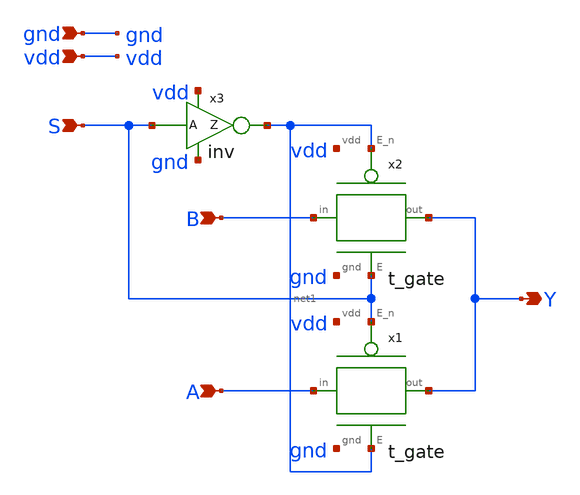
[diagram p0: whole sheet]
** sch_path: xschem/mux21.sch
**.subckt mux21 S A B Y vdd gnd
*.ipin S
*.ipin A
*.ipin B
*.opin Y
*.ipin vdd
*.ipin gnd
x1 S A Y net1 vdd gnd t_gate
x2 net1 B Y S vdd gnd t_gate
x3 net1 S vdd gnd inv
**.ends

* expanding   symbol:  t_gate.sym # of pins=6
** sym_path: xschem/t_gate.sym
** sch_path: xschem/t_gate.sch
.subckt t_gate E_n in out E vdd gnd
*.ipin in
*.opin out
*.ipin E
*.ipin E_n
*.ipin vdd
*.ipin gnd
XM1 in E out gnd sky130_fd_pr__nfet_01v8 L=0.15 W=0.42 nf=1 ad='int((nf+1)/2) * W/nf * 0.29' as='int((nf+2)/2) * W/nf * 0.29'
+ pd='2*int((nf+1)/2) * (W/nf + 0.29)' ps='2*int((nf+2)/2) * (W/nf + 0.29)' nrd='0.29 / W' nrs='0.29 / W'
+ sa=0 sb=0 sd=0 mult=1 m=1
XM2 in E_n out vdd sky130_fd_pr__pfet_01v8 L=0.15 W=0.84 nf=1 ad='int((nf+1)/2) * W/nf * 0.29' as='int((nf+2)/2) * W/nf * 0.29'
+ pd='2*int((nf+1)/2) * (W/nf + 0.29)' ps='2*int((nf+2)/2) * (W/nf + 0.29)' nrd='0.29 / W' nrs='0.29 / W'
+ sa=0 sb=0 sd=0 mult=1 m=1
.ends


* expanding   symbol:  inv.sym # of pins=4
** sym_path: xschem/inv.sym
** sch_path: xschem/inv.sch
.subckt inv Z A vdd gnd
*.ipin A
*.opin Z
*.ipin vdd
*.ipin gnd
XM1 Z A gnd GND sky130_fd_pr__nfet_01v8 L=0.15 W=0.42 nf=1 ad='int((nf+1)/2) * W/nf * 0.29' as='int((nf+2)/2) * W/nf * 0.29'
+ pd='2*int((nf+1)/2) * (W/nf + 0.29)' ps='2*int((nf+2)/2) * (W/nf + 0.29)' nrd='0.29 / W' nrs='0.29 / W'
+ sa=0 sb=0 sd=0 mult=1 m=1
XM2 Z A vdd VDD sky130_fd_pr__pfet_01v8 L=0.15 W=0.84 nf=1 ad='int((nf+1)/2) * W/nf * 0.29' as='int((nf+2)/2) * W/nf * 0.29'
+ pd='2*int((nf+1)/2) * (W/nf + 0.29)' ps='2*int((nf+2)/2) * (W/nf + 0.29)' nrd='0.29 / W' nrs='0.29 / W'
+ sa=0 sb=0 sd=0 mult=1 m=1
.ends

.end
